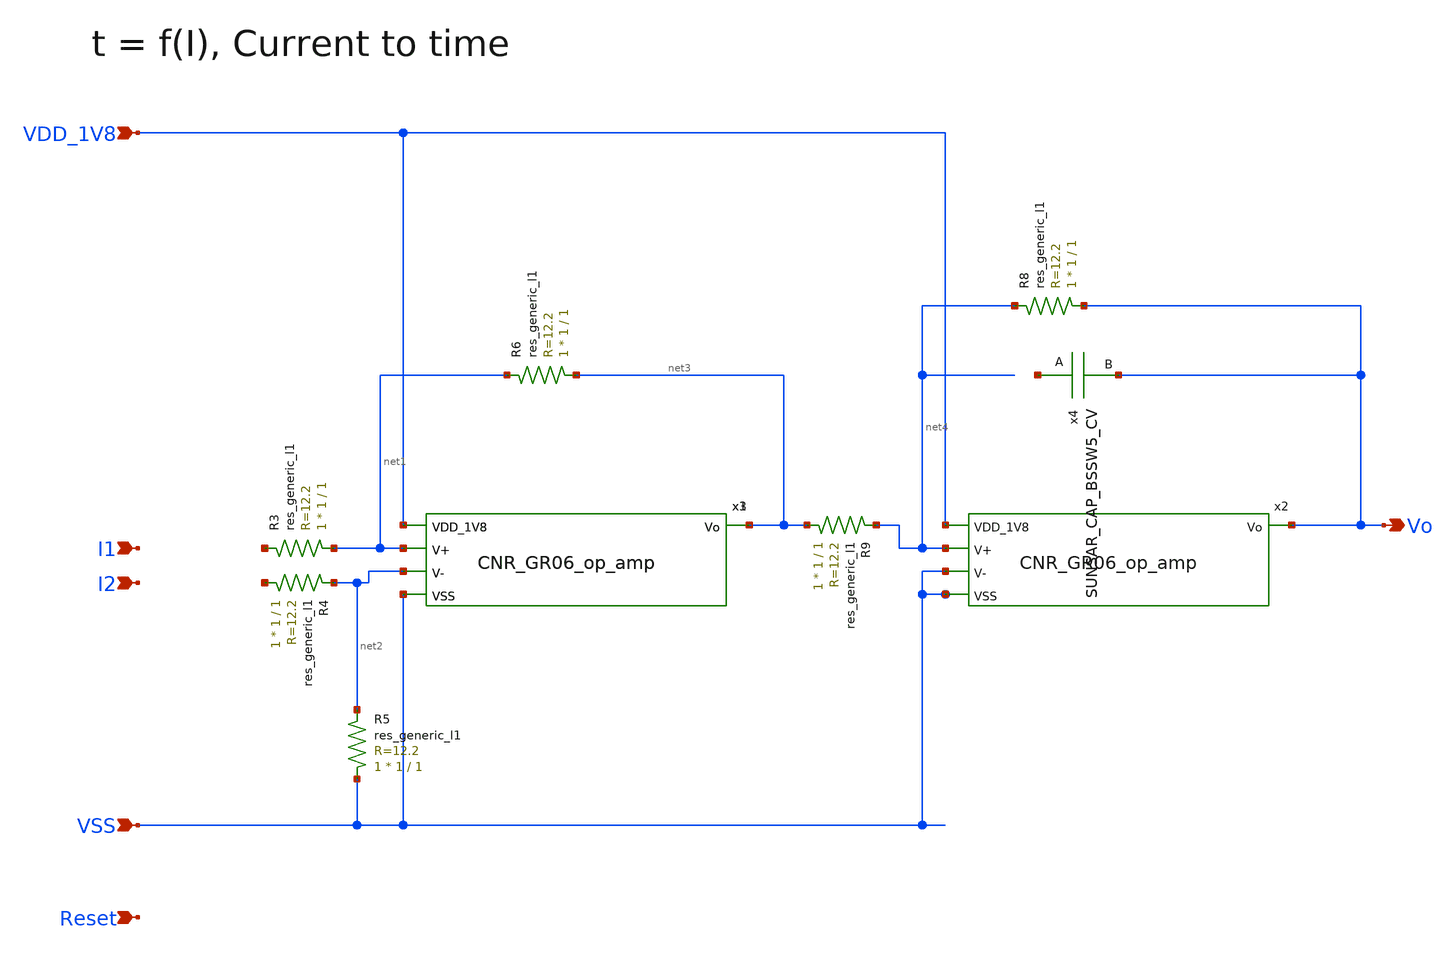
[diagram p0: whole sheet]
** sch_path: design/CNR_GR06_SKY130NM/CNR_GR06_I_to_t.sch
**.subckt CNR_GR06_I_to_t I2 VDD_1V8 VSS I1 Reset Vo
*.ipin I2
*.ipin VDD_1V8
*.ipin VSS
*.ipin I1
*.ipin Reset
*.opin Vo
x1 VDD_1V8 net3 net1 net2 VSS CNR_GR06_op_amp
x2 VDD_1V8 Vo net4 VSS VSS CNR_GR06_op_amp
x3 VDD_1V8 net3 net1 net2 VSS CNR_GR06_op_amp
R3 net1 net5 sky130_fd_pr__res_generic_l1 W=1 L=1 m=1
R4 net6 net2 sky130_fd_pr__res_generic_l1 W=1 L=1 m=1
R5 VSS net2 sky130_fd_pr__res_generic_l1 W=1 L=1 m=1
R6 net3 net1 sky130_fd_pr__res_generic_l1 W=1 L=1 m=1
R8 Vo net4 sky130_fd_pr__res_generic_l1 W=1 L=1 m=1
R9 net3 net4 sky130_fd_pr__res_generic_l1 W=1 L=1 m=1
x4 net7 Vo SUNSAR_CAP_BSSW5_CV
**.ends
.end
